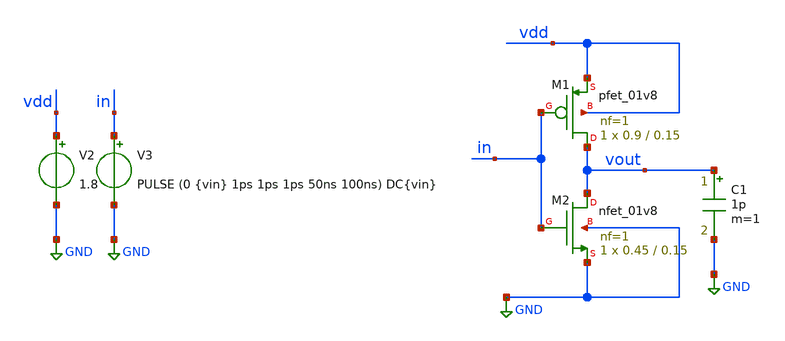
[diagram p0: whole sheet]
** sch_path: track_vlsi/lado/sch/testbench.sch
**.subckt testbench
V2 vdd GND 1.8
V3 in GND PULSE (0 {vin} 1ps 1ps 1ps 50ns 100ns) DC{vin}
C1 vout GND 1p m=1
XM1 vout in vdd vdd sky130_fd_pr__pfet_01v8 L=0.15 W=0.9 nf=1 ad='int((nf+1)/2) * W/nf * 0.29' as='int((nf+2)/2) * W/nf * 0.29'
+ pd='2*int((nf+1)/2) * (W/nf + 0.29)' ps='2*int((nf+2)/2) * (W/nf + 0.29)' nrd='0.29 / W' nrs='0.29 / W'
+ sa=0 sb=0 sd=0 mult=1 m=1
XM2 vout in GND GND sky130_fd_pr__nfet_01v8 L=0.15 W=0.45 nf=1 ad='int((nf+1)/2) * W/nf * 0.29' as='int((nf+2)/2) * W/nf * 0.29'
+ pd='2*int((nf+1)/2) * (W/nf + 0.29)' ps='2*int((nf+2)/2) * (W/nf + 0.29)' nrd='0.29 / W' nrs='0.29 / W'
+ sa=0 sb=0 sd=0 mult=1 m=1
**** begin user architecture code



*parametros
.param vin=1.8
.options TEMP=27.0

*include

.lib /home/eamta/skywater/skywater-pdk/libraries/sky130_fd_pr_ngspice/latest/models/corners/sky130.lib TT

*signals to save
.save all
*+ @m.x1.xm2.msky130_fd_pr__nfet_01v8[id] @m.x1.xm2.msky130_fd_pr__nfet_01v8[gm]
*+ @m.x1.xm1.msky130_fd_pr__pfet_01v8[id] @m.x1.xm1.msky130_fd_pr__pfet_01v8[gm]




*config simulacion

.control
  tran 0.1ns 0.5us
  setplot tran1
  plot v(vout) v(in)
  write tb_inverter_trans.raw

  reset
  dc V3 0 1.8 0.01
  setplot dc1
  plot v(vout) v(in)
  write tb_inverter_dc.raw
  gnuplot salida v(vout) v(in)
  reset
  op
  print all


.endc


.end




**** end user architecture code
**.ends
.GLOBAL GND
.end
